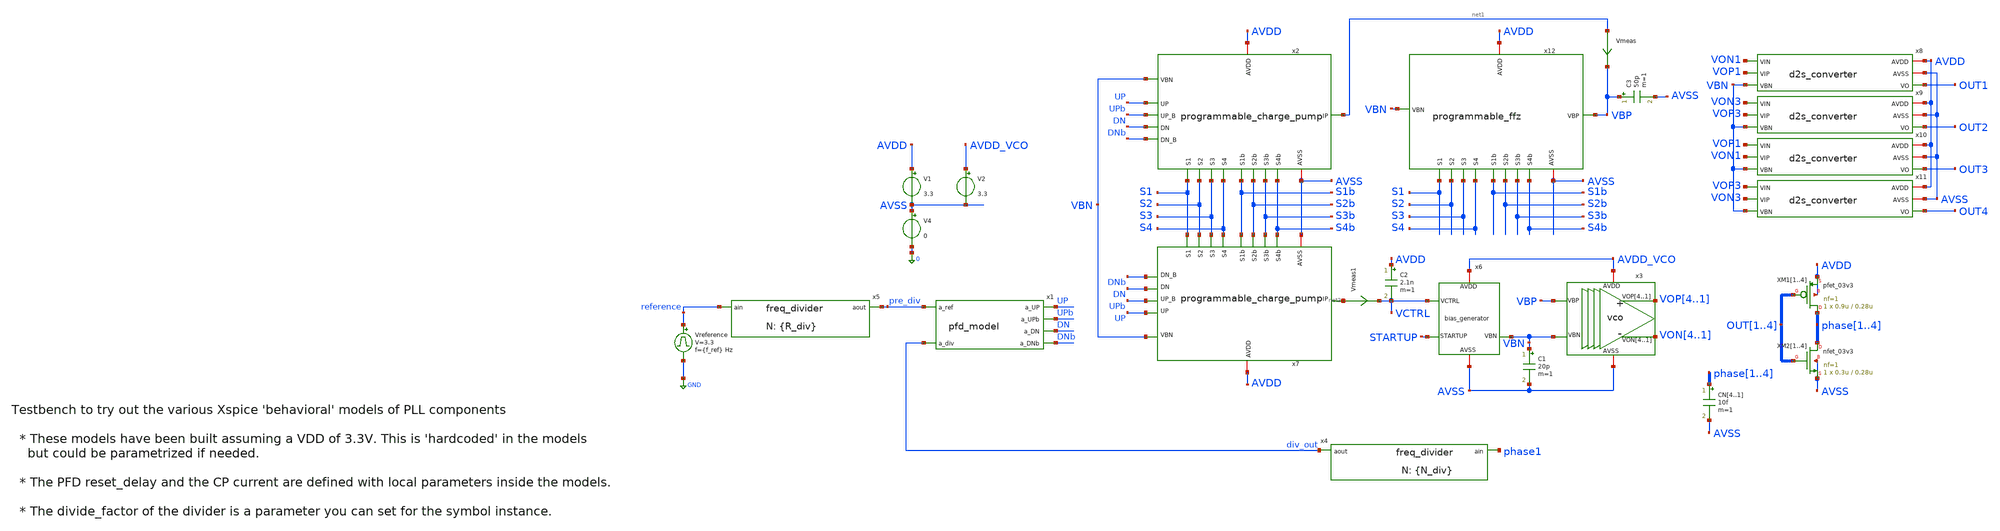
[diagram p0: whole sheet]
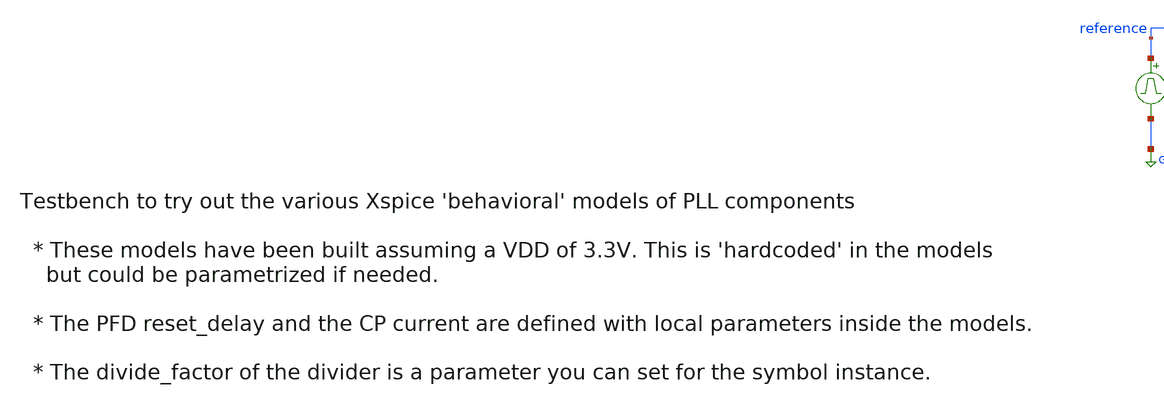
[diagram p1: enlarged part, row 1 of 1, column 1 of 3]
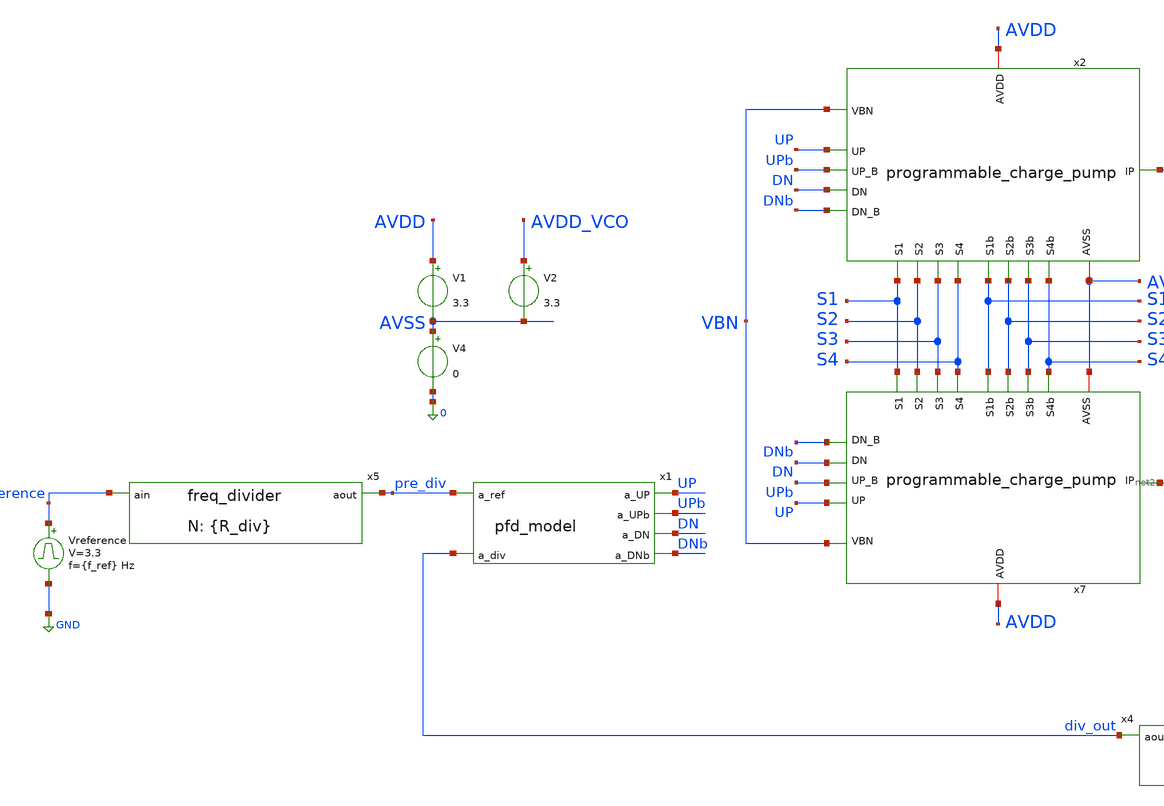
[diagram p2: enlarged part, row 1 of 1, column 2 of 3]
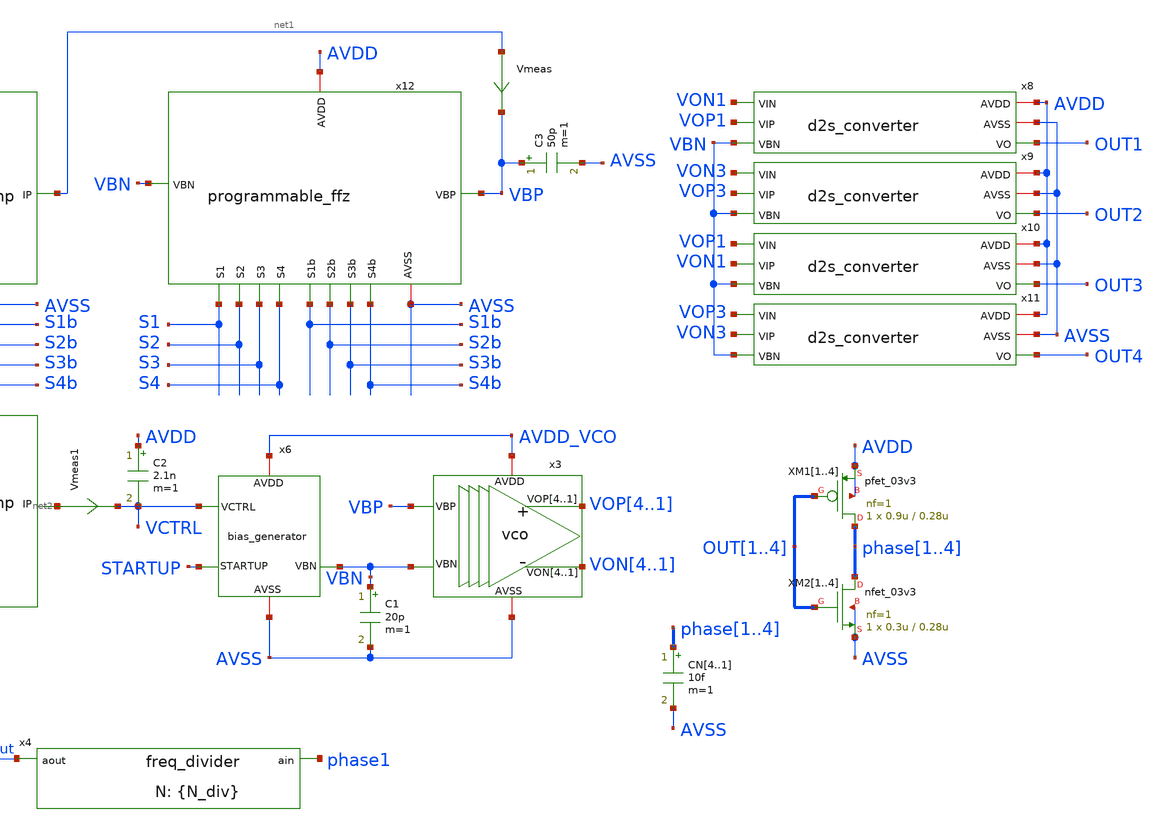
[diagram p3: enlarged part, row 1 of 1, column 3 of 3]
** sch_path: designs/libs/tb_pll/tb_PLL_CP_VCO_model.sch
**.subckt tb_PLL_CP_VCO_model
Vreference reference GND pulse 0 3.3 '0.495/ {f_ref} ' '0.01/{f_ref} ' '0.01/{f_ref} ' '0.49/{f_ref} '
+ '1/{f_ref} '
x1 pre_div UP UPb DN div_out DNb pfd_model
x4 div_out phase1 freq_divider divide_factor={N_div}
x5 pre_div reference freq_divider divide_factor={R_div}
x3 VOP4 VOP3 VOP2 VOP1 VON4 VON3 VON2 VON1 AVDD_VCO AVSS VBP VBN vco
x6 VCTRL AVDD_VCO STARTUP AVSS VBN bias_generator
C2 AVDD VCTRL 2.1n m=1
x8 AVDD AVSS VON1 VOP1 VBN OUT1 d2s_converter
XM11 phase1 OUT1 AVDD AVDD pfet_03v3 L=0.28u W=0.9u nf=1 ad='int((nf+1)/2) * W/nf * 0.18u' as='int((nf+2)/2) * W/nf * 0.18u'
+ pd='2*int((nf+1)/2) * (W/nf + 0.18u)' ps='2*int((nf+2)/2) * (W/nf + 0.18u)' nrd='0.18u / W' nrs='0.18u / W'
+ sa=0 sb=0 sd=0 m=1
XM12 phase2 OUT2 AVDD AVDD pfet_03v3 L=0.28u W=0.9u nf=1 ad='int((nf+1)/2) * W/nf * 0.18u' as='int((nf+2)/2) * W/nf * 0.18u'
+ pd='2*int((nf+1)/2) * (W/nf + 0.18u)' ps='2*int((nf+2)/2) * (W/nf + 0.18u)' nrd='0.18u / W' nrs='0.18u / W'
+ sa=0 sb=0 sd=0 m=1
XM13 phase3 OUT3 AVDD AVDD pfet_03v3 L=0.28u W=0.9u nf=1 ad='int((nf+1)/2) * W/nf * 0.18u' as='int((nf+2)/2) * W/nf * 0.18u'
+ pd='2*int((nf+1)/2) * (W/nf + 0.18u)' ps='2*int((nf+2)/2) * (W/nf + 0.18u)' nrd='0.18u / W' nrs='0.18u / W'
+ sa=0 sb=0 sd=0 m=1
XM14 phase4 OUT4 AVDD AVDD pfet_03v3 L=0.28u W=0.9u nf=1 ad='int((nf+1)/2) * W/nf * 0.18u' as='int((nf+2)/2) * W/nf * 0.18u'
+ pd='2*int((nf+1)/2) * (W/nf + 0.18u)' ps='2*int((nf+2)/2) * (W/nf + 0.18u)' nrd='0.18u / W' nrs='0.18u / W'
+ sa=0 sb=0 sd=0 m=1
XM21 phase1 OUT1 AVSS AVSS nfet_03v3 L=0.28u W=0.3u nf=1 ad='int((nf+1)/2) * W/nf * 0.18u' as='int((nf+2)/2) * W/nf * 0.18u'
+ pd='2*int((nf+1)/2) * (W/nf + 0.18u)' ps='2*int((nf+2)/2) * (W/nf + 0.18u)' nrd='0.18u / W' nrs='0.18u / W'
+ sa=0 sb=0 sd=0 m=1
XM22 phase2 OUT2 AVSS AVSS nfet_03v3 L=0.28u W=0.3u nf=1 ad='int((nf+1)/2) * W/nf * 0.18u' as='int((nf+2)/2) * W/nf * 0.18u'
+ pd='2*int((nf+1)/2) * (W/nf + 0.18u)' ps='2*int((nf+2)/2) * (W/nf + 0.18u)' nrd='0.18u / W' nrs='0.18u / W'
+ sa=0 sb=0 sd=0 m=1
XM23 phase3 OUT3 AVSS AVSS nfet_03v3 L=0.28u W=0.3u nf=1 ad='int((nf+1)/2) * W/nf * 0.18u' as='int((nf+2)/2) * W/nf * 0.18u'
+ pd='2*int((nf+1)/2) * (W/nf + 0.18u)' ps='2*int((nf+2)/2) * (W/nf + 0.18u)' nrd='0.18u / W' nrs='0.18u / W'
+ sa=0 sb=0 sd=0 m=1
XM24 phase4 OUT4 AVSS AVSS nfet_03v3 L=0.28u W=0.3u nf=1 ad='int((nf+1)/2) * W/nf * 0.18u' as='int((nf+2)/2) * W/nf * 0.18u'
+ pd='2*int((nf+1)/2) * (W/nf + 0.18u)' ps='2*int((nf+2)/2) * (W/nf + 0.18u)' nrd='0.18u / W' nrs='0.18u / W'
+ sa=0 sb=0 sd=0 m=1
x9 AVDD AVSS VON3 VOP3 VBN OUT2 d2s_converter
x10 AVDD AVSS VOP1 VON1 VBN OUT3 d2s_converter
x11 AVDD AVSS VOP3 VON3 VBN OUT4 d2s_converter
V1 AVDD AVSS 3.3
V4 AVSS 0 0
V2 AVDD_VCO AVSS 3.3
x2 AVSS AVDD UP UPb DN net1 DNb VBN S1b S1 S2b S2 S3b S3 S4b S4 programmable_charge_pump
x7 AVSS AVDD UP UPb DN net2 DNb VBN S1b S1 S2b S2 S3b S3 S4b S4 programmable_charge_pump
CN4 phase1 AVSS 10f m=1
CN3 phase2 AVSS 10f m=1
CN2 phase3 AVSS 10f m=1
CN1 phase4 AVSS 10f m=1
Vmeas net1 VBP 0
.save i(vmeas)
Vmeas1 net2 VCTRL 0
.save i(vmeas1)
C1 VBN AVSS 20p m=1
C3 VBP AVSS 50p m=1
x12 VBP AVSS AVDD VBN S1b S1 S2b S2 S3b S3 S4b S4 programmable_ffz
**** begin user architecture code


.param f_ref=2MEG R_div=2 N_div=255
*.param f_ref=2e3 R_div=2 N_div=255
.param tp_ref='1/f_ref' td_ref='tp_ref*2'
Vref reference gnd pulse(0 3.3 0 10p 10p tp_ref td_ref)

*.ic v(VCTRL)=2.6 v(vbp)=2.6
.ic v(VCTRL)=1 v(vbp)=1

.ic v(vop1)=3.3 v(von1)=0 v(startup)=0
.options reltol=1e-5 cshunt=1e-15
.options method=gear

.param d1=0 d2=0 d3=0 d4=0
.param d1b=3.3 d2b=3.3 d3b=3.3 d4b=3.3

*.param d1=3.3 d2=3.3 d3=3.3 d4=3.3
*.param d1b=0 d2b=0 d3b=0 d4b=0

VS1 S1 0 d1
VS2 S2 0 d2
VS3 S3 0 d3
VS4 S4 0 d4

VS1b S1b 0 d1b
VS2b S2b 0 d2b
VS3b S3b 0 d3b
VS4b S4b 0 d4b

.control
set wr_singlescale
set wr_vecnames

* save all
save v(VCTRL) v(vbp) v(vbn) v(reference) v(div_out) v(pre_div) v(phase1) v(phase2) v(phase3)
+ v(phase4) v(up) v(dn)

*v(vop1) v(von1) v(vop3) v(von3)

*OP
*show all

*tran 100n 70m
tran 0.1n 100u

remzerovec

*tran 1
*write tb_PLL_CP_VCO_model_R2_N2_350MEG.raw
*tran 2
write tb_PLL_CP_VCO_model_R2_N255_255MEG.raw

*tran 3
*write tb_PLL_CP_VCO_model_R2_N2_50kHz.raw
*tran 4
*write tb_PLL_CP_VCO_model_R2_N255_255kHz.raw
*write tb_PLL_CP_VCO_model_R2_N200_200kHz.raw
wrdata
+ /foss/designs/synchronos-chipathon-2026/designs/libs/scripts/sim_data/tb_PLL_CP_VCO_model_R2_N255_255MEG.txt tran.all
*tran 5

*tran 6

*tran 8

*tran 10

.endc



.include $::180MCU_MODELS/design.ngspice
.lib $::180MCU_MODELS/sm141064.ngspice typical
*.lib $::180MCU_MODELS/sm141064.ngspice SS
*.lib $::180MCU_MODELS/sm141064.ngspice FF
*.lib $::180MCU_MODELS/sm141064.ngspice SF
*.lib $::180MCU_MODELS/sm141064.ngspice FS

**** end user architecture code
**.ends

* expanding   symbol:  libs/model_pll/pfd_model.sym # of pins=6
** sym_path: designs/libs/model_pll/pfd_model.sym
** sch_path: designs/libs/model_pll/pfd_model.sch
.subckt pfd_model a_ref a_UP a_UPb a_DN a_div a_DNb
*.ipin a_ref
*.ipin a_div
*.opin a_UP
*.opin a_UPb
*.opin a_DN
*.opin a_DNb
* noconn a_ref
* noconn a_div
* noconn a_UP
* noconn a_UPb
* noconn a_DN
* noconn a_DNb
**** begin user architecture code


* PFD Model using digital Xspice components

* pfd_delay local parameter sets the duration of the overlap (dead-band elimination)
* Reduced from 10ns to 200ps to prevent massive Vctrl ripple
*.param pfd_delay = 200p
.param pfd_delay = 1.5n

** Digital 1 and 0 to drive Flip-Flops
aone 0 d_d1 d_inv
azero d_d1 d_d0 d_inv
.model d_inv d_inverter()

** Flip Flops
ad1 d_d1 d_R d_d0 d_rset d_U d_U_ flop1
ad2 d_d1 d_V d_d0 d_rset d_D d_D_ flop1
.model flop1 d_dff(clk_delay = 1.0e-10 set_delay = 1.0e-10  reset_delay = {pfd_delay} ic = 2 rise_delay
+ = 1.0e-10  fall_delay = 1e-10)

* AND Gate
aa1 [d_U d_D] d_rset and1
.model and1 d_and(rise_delay = 1e-10 fall_delay = 1e-10   input_load = 0.5e-12)

* WINDOW FIX: Widened thresholds to catch fast analog edges safely
aADC [ a_ref a_div ] [ d_R d_V ] adc_buff
.model adc_buff adc_bridge(in_low = 1.2 in_high = 2.1 rise_delay = 10p fall_delay = 10p)

* DAC FIX: Explicitly defined analog rise/fall times to prevent solver crashes
aDAC [ d_U d_U_ d_D d_D_ d_rset d_R d_V d_d1 d_d0 ] [ a_UP a_UPb a_DN a_DNb a_rset a_R a_V a_d1
+ a_d0] dac_buff
.model dac_buff dac_bridge(out_low = 0 out_high = 3.3 t_rise = 500p t_fall = 500p)


**** end user architecture code
.ends


* expanding   symbol:  libs/model_pll/freq_divider.sym # of pins=2
** sym_path: libs/model_pll/freq_divider.sym
** sch_path: libs/model_pll/freq_divider.sch
.subckt freq_divider aout ain  divide_factor=20
*.ipin ain
*.opin aout
* noconn ain
* noconn aout
**** begin user architecture code


* Behavioral Frequency Divider with robust Mixed-Signal Bridges

* Top-level parameter (Defaults to 10 if not passed by symbol)
.param divide_factor = 10

* MATH FIX: Guarantees at least 1 high cycle, targets 50% duty cycle
.param high_cycles = {max(1, floor(divide_factor/2))}

* Xspice digital frequency divider
adiv din dout divider
.model divider d_fdiv(div_factor = {divide_factor}  high_cycles = {high_cycles}  i_count = 0  rise_delay
+ = 10p fall_delay = 10p )

* WINDOW FIX: Widened analog-to-digital thresholds to catch fast sine waves
aADC [ ain ] [ din ] adc_buff
.model adc_buff adc_bridge(in_low = 1.2 in_high = 2.1 rise_delay = 10p fall_delay = 10p)

* Digital-to-analog bridge
aDAC [ dout ] [ aout ] dac_buff
.model dac_buff dac_bridge(out_low = 0 out_high = 3.3 t_rise = 10p t_fall = 10p)


**** end user architecture code
.ends


* expanding   symbol:  libs/core_analog/vco/vco.sym # of pins=6
** sym_path: designs/libs/core_analog/vco/vco.sym
** sch_path: designs/libs/core_analog/vco/vco.sch
.subckt vco VOP4 VOP3 VOP2 VOP1 VON4 VON3 VON2 VON1 AVDD AVSS VBP VBN
*.opin VOP1,VOP2,VOP3,VOP4
*.opin VON1,VON2,VON3,VON4
*.ipin VBP
*.ipin VBN
*.iopin AVDD
*.iopin AVSS
x1 VOP1 AVDD VOP4 VON4 VON1 AVSS VBP VBN delay_stage
x2 VOP2 AVDD VON1 VOP1 VON2 AVSS VBP VBN delay_stage
x3 VOP3 AVDD VON2 VOP2 VON3 AVSS VBP VBN delay_stage
x4 VOP4 AVDD VON3 VOP3 VON4 AVSS VBP VBN delay_stage
.ends


* expanding   symbol:  libs/core_analog/bias_generator/bias_generator.sym # of pins=5
** sym_path: designs/libs/core_analog/bias_generator/bias_generator.sym
** sch_path: designs/libs/core_analog/bias_generator/bias_generator.sch
.subckt bias_generator VCTRL AVDD STARTUP AVSS VBN
*.ipin VCTRL
*.ipin STARTUP
*.iopin AVDD
*.iopin AVSS
*.opin VBN
x1 VBN AVDD net2 VCTRL AVSS net1 ota_5t
XM1 net1 net1 AVDD AVDD pfet_03v3 L=0.5u W=16.8u nf=1 ad='int((nf+1)/2) * W/nf * 0.18u' as='int((nf+2)/2) * W/nf * 0.18u'
+ pd='2*int((nf+1)/2) * (W/nf + 0.18u)' ps='2*int((nf+2)/2) * (W/nf + 0.18u)' nrd='0.18u / W' nrs='0.18u / W'
+ sa=0 sb=0 sd=0 m=16
XM8 net2 AVDD net4 AVSS nfet_03v3 L=0.5u W=2.08u nf=1 ad='int((nf+1)/2) * W/nf * 0.18u' as='int((nf+2)/2) * W/nf * 0.18u'
+ pd='2*int((nf+1)/2) * (W/nf + 0.18u)' ps='2*int((nf+2)/2) * (W/nf + 0.18u)' nrd='0.18u / W' nrs='0.18u / W'
+ sa=0 sb=0 sd=0 m=8
XM11 net1 AVDD net3 AVSS nfet_03v3 L=0.5u W=2.08u nf=1 ad='int((nf+1)/2) * W/nf * 0.18u' as='int((nf+2)/2) * W/nf * 0.18u'
+ pd='2*int((nf+1)/2) * (W/nf + 0.18u)' ps='2*int((nf+2)/2) * (W/nf + 0.18u)' nrd='0.18u / W' nrs='0.18u / W'
+ sa=0 sb=0 sd=0 m=8
XM3 net4 VBN AVSS AVSS nfet_03v3 L=0.5u W=11.25u nf=1 ad='int((nf+1)/2) * W/nf * 0.18u' as='int((nf+2)/2) * W/nf * 0.18u'
+ pd='2*int((nf+1)/2) * (W/nf + 0.18u)' ps='2*int((nf+2)/2) * (W/nf + 0.18u)' nrd='0.18u / W' nrs='0.18u / W'
+ sa=0 sb=0 sd=0 m=8
XM4 net3 VBN AVSS AVSS nfet_03v3 L=0.5u W=11.25u nf=1 ad='int((nf+1)/2) * W/nf * 0.18u' as='int((nf+2)/2) * W/nf * 0.18u'
+ pd='2*int((nf+1)/2) * (W/nf + 0.18u)' ps='2*int((nf+2)/2) * (W/nf + 0.18u)' nrd='0.18u / W' nrs='0.18u / W'
+ sa=0 sb=0 sd=0 m=8
XM10 net3 STARTUP AVSS AVSS nfet_03v3 L=0.5u W=11.25u nf=1 ad='int((nf+1)/2) * W/nf * 0.18u' as='int((nf+2)/2) * W/nf * 0.18u'
+ pd='2*int((nf+1)/2) * (W/nf + 0.18u)' ps='2*int((nf+2)/2) * (W/nf + 0.18u)' nrd='0.18u / W' nrs='0.18u / W'
+ sa=0 sb=0 sd=0 m=8
XM2 net2 VCTRL AVDD AVDD pfet_03v3 L=1.5u W=1.1u nf=1 ad='int((nf+1)/2) * W/nf * 0.18u' as='int((nf+2)/2) * W/nf * 0.18u'
+ pd='2*int((nf+1)/2) * (W/nf + 0.18u)' ps='2*int((nf+2)/2) * (W/nf + 0.18u)' nrd='0.18u / W' nrs='0.18u / W'
+ sa=0 sb=0 sd=0 m=8
XM5 net2 net2 AVDD AVDD pfet_03v3 L=1.5u W=1.1u nf=1 ad='int((nf+1)/2) * W/nf * 0.18u' as='int((nf+2)/2) * W/nf * 0.18u'
+ pd='2*int((nf+1)/2) * (W/nf + 0.18u)' ps='2*int((nf+2)/2) * (W/nf + 0.18u)' nrd='0.18u / W' nrs='0.18u / W'
+ sa=0 sb=0 sd=0 m=8
.ends


* expanding   symbol:  libs/core_analog/d2s_converter/d2s_converter.sym # of pins=6
** sym_path: designs/libs/core_analog/d2s_converter/d2s_converter.sym
** sch_path: designs/libs/core_analog/d2s_converter/d2s_converter.sch
.subckt d2s_converter AVDD AVSS VIN VIP VBN VO
*.iopin AVDD
*.iopin AVSS
*.ipin VIN
*.ipin VIP
*.opin VO
*.ipin VBN
XM2 VOPB VIN i1 AVSS nfet_03v3 L=0.3u W=1.9u nf=1 ad='int((nf+1)/2) * W/nf * 0.18u' as='int((nf+2)/2) * W/nf * 0.18u'
+ pd='2*int((nf+1)/2) * (W/nf + 0.18u)' ps='2*int((nf+2)/2) * (W/nf + 0.18u)' nrd='0.18u / W' nrs='0.18u / W'
+ sa=0 sb=0 sd=0 m=4
XM4 VOPB VOPB AVDD AVDD pfet_03v3 L=0.3u W=1.4u nf=1 ad='int((nf+1)/2) * W/nf * 0.18u' as='int((nf+2)/2) * W/nf * 0.18u'
+ pd='2*int((nf+1)/2) * (W/nf + 0.18u)' ps='2*int((nf+2)/2) * (W/nf + 0.18u)' nrd='0.18u / W' nrs='0.18u / W'
+ sa=0 sb=0 sd=0 m=4
XM11 VOB VOB AVSS AVSS nfet_03v3 L=0.3u W=1.5u nf=1 ad='int((nf+1)/2) * W/nf * 0.18u' as='int((nf+2)/2) * W/nf * 0.18u'
+ pd='2*int((nf+1)/2) * (W/nf + 0.18u)' ps='2*int((nf+2)/2) * (W/nf + 0.18u)' nrd='0.18u / W' nrs='0.18u / W'
+ sa=0 sb=0 sd=0 m=4
XM13 VOB VOP AVDD AVDD pfet_03v3 L=0.3u W=2u nf=1 ad='int((nf+1)/2) * W/nf * 0.18u' as='int((nf+2)/2) * W/nf * 0.18u'
+ pd='2*int((nf+1)/2) * (W/nf + 0.18u)' ps='2*int((nf+2)/2) * (W/nf + 0.18u)' nrd='0.18u / W' nrs='0.18u / W'
+ sa=0 sb=0 sd=0 m=4
XM3 VOP VIP i1 AVSS nfet_03v3 L=0.3u W=1.9u nf=1 ad='int((nf+1)/2) * W/nf * 0.18u' as='int((nf+2)/2) * W/nf * 0.18u'
+ pd='2*int((nf+1)/2) * (W/nf + 0.18u)' ps='2*int((nf+2)/2) * (W/nf + 0.18u)' nrd='0.18u / W' nrs='0.18u / W'
+ sa=0 sb=0 sd=0 m=4
XM5 VOP VOPB AVDD AVDD pfet_03v3 L=0.3u W=1.4u nf=1 ad='int((nf+1)/2) * W/nf * 0.18u' as='int((nf+2)/2) * W/nf * 0.18u'
+ pd='2*int((nf+1)/2) * (W/nf + 0.18u)' ps='2*int((nf+2)/2) * (W/nf + 0.18u)' nrd='0.18u / W' nrs='0.18u / W'
+ sa=0 sb=0 sd=0 m=4
XM7 VONB VIP i2 AVSS nfet_03v3 L=0.3u W=1.9u nf=1 ad='int((nf+1)/2) * W/nf * 0.18u' as='int((nf+2)/2) * W/nf * 0.18u'
+ pd='2*int((nf+1)/2) * (W/nf + 0.18u)' ps='2*int((nf+2)/2) * (W/nf + 0.18u)' nrd='0.18u / W' nrs='0.18u / W'
+ sa=0 sb=0 sd=0 m=4
XM8 VONB VONB AVDD AVDD pfet_03v3 L=0.3u W=1.4u nf=1 ad='int((nf+1)/2) * W/nf * 0.18u' as='int((nf+2)/2) * W/nf * 0.18u'
+ pd='2*int((nf+1)/2) * (W/nf + 0.18u)' ps='2*int((nf+2)/2) * (W/nf + 0.18u)' nrd='0.18u / W' nrs='0.18u / W'
+ sa=0 sb=0 sd=0 m=4
XM9 VON VIN i2 AVSS nfet_03v3 L=0.3u W=1.9u nf=1 ad='int((nf+1)/2) * W/nf * 0.18u' as='int((nf+2)/2) * W/nf * 0.18u'
+ pd='2*int((nf+1)/2) * (W/nf + 0.18u)' ps='2*int((nf+2)/2) * (W/nf + 0.18u)' nrd='0.18u / W' nrs='0.18u / W'
+ sa=0 sb=0 sd=0 m=4
XM10 VON VONB AVDD AVDD pfet_03v3 L=0.3u W=1.4u nf=1 ad='int((nf+1)/2) * W/nf * 0.18u' as='int((nf+2)/2) * W/nf * 0.18u'
+ pd='2*int((nf+1)/2) * (W/nf + 0.18u)' ps='2*int((nf+2)/2) * (W/nf + 0.18u)' nrd='0.18u / W' nrs='0.18u / W'
+ sa=0 sb=0 sd=0 m=4
XM14 VO VON AVDD AVDD pfet_03v3 L=0.3u W=2u nf=1 ad='int((nf+1)/2) * W/nf * 0.18u' as='int((nf+2)/2) * W/nf * 0.18u'
+ pd='2*int((nf+1)/2) * (W/nf + 0.18u)' ps='2*int((nf+2)/2) * (W/nf + 0.18u)' nrd='0.18u / W' nrs='0.18u / W'
+ sa=0 sb=0 sd=0 m=4
XM12 VO VOB AVSS AVSS nfet_03v3 L=0.3u W=1.5u nf=1 ad='int((nf+1)/2) * W/nf * 0.18u' as='int((nf+2)/2) * W/nf * 0.18u'
+ pd='2*int((nf+1)/2) * (W/nf + 0.18u)' ps='2*int((nf+2)/2) * (W/nf + 0.18u)' nrd='0.18u / W' nrs='0.18u / W'
+ sa=0 sb=0 sd=0 m=4
XM1 i1 VBN AVSS AVSS nfet_03v3 L=0.5u W=11.25u nf=1 ad='int((nf+1)/2) * W/nf * 0.18u' as='int((nf+2)/2) * W/nf * 0.18u'
+ pd='2*int((nf+1)/2) * (W/nf + 0.18u)' ps='2*int((nf+2)/2) * (W/nf + 0.18u)' nrd='0.18u / W' nrs='0.18u / W'
+ sa=0 sb=0 sd=0 m=4
XM6 i2 VBN AVSS AVSS nfet_03v3 L=0.5u W=11.25u nf=1 ad='int((nf+1)/2) * W/nf * 0.18u' as='int((nf+2)/2) * W/nf * 0.18u'
+ pd='2*int((nf+1)/2) * (W/nf + 0.18u)' ps='2*int((nf+2)/2) * (W/nf + 0.18u)' nrd='0.18u / W' nrs='0.18u / W'
+ sa=0 sb=0 sd=0 m=4
.ends


* expanding   symbol:  libs/core_analog/programmable_charge_pump/programmable_charge_pump.sym # of
*+ pins=16
** sym_path: designs/libs/core_analog/programmable_charge_pump/programmable_charge_pump.sym
** sch_path: designs/libs/core_analog/programmable_charge_pump/programmable_charge_pump.sch
.subckt programmable_charge_pump AVSS AVDD UP UP_B DN IP DN_B VBN S1b S1 S2b S2 S3b S3 S4b S4
*.ipin VBN
*.ipin S1b
*.ipin S1
*.ipin S2b
*.ipin S2
*.ipin S3b
*.ipin S3
*.ipin S4b
*.ipin S4
*.iopin AVSS
*.iopin AVDD
*.ipin UP
*.ipin UP_B
*.ipin DN
*.ipin DN_B
*.opin IP
x1 AVDD AVSS UP UP_B DN DN_B VBN1 IP S1b charge_pump
x61 AVDD AVSS UP UP_B DN DN_B VBN2 IP S2b charge_pump
x62 AVDD AVSS UP UP_B DN DN_B VBN2 IP S2b charge_pump
x71 AVDD AVSS UP UP_B DN DN_B VBN3 IP S3b charge_pump
x72 AVDD AVSS UP UP_B DN DN_B VBN3 IP S3b charge_pump
x73 AVDD AVSS UP UP_B DN DN_B VBN3 IP S3b charge_pump
x74 AVDD AVSS UP UP_B DN DN_B VBN3 IP S3b charge_pump
x81 AVDD AVSS UP UP_B DN DN_B VBN4 IP S4b charge_pump
x82 AVDD AVSS UP UP_B DN DN_B VBN4 IP S4b charge_pump
x83 AVDD AVSS UP UP_B DN DN_B VBN4 IP S4b charge_pump
x84 AVDD AVSS UP UP_B DN DN_B VBN4 IP S4b charge_pump
x85 AVDD AVSS UP UP_B DN DN_B VBN4 IP S4b charge_pump
x86 AVDD AVSS UP UP_B DN DN_B VBN4 IP S4b charge_pump
x87 AVDD AVSS UP UP_B DN DN_B VBN4 IP S4b charge_pump
x88 AVDD AVSS UP UP_B DN DN_B VBN4 IP S4b charge_pump
x2 VBN AVSS S1 VBN1 S1b AVDD transmission_gate
x0 AVDD AVSS UP UP_B DN DN_B VBN IP AVSS charge_pump
x3 VBN AVSS S2 VBN2 S2b AVDD transmission_gate
x4 VBN AVSS S3 VBN3 S3b AVDD transmission_gate
x5 VBN AVSS S4 VBN4 S4b AVDD transmission_gate
.ends


* expanding   symbol:  libs/core_analog/programmable_ffz/programmable_ffz.sym # of pins=12
** sym_path: designs/libs/core_analog/programmable_ffz/programmable_ffz.sym
** sch_path: designs/libs/core_analog/programmable_ffz/programmable_ffz.sch
.subckt programmable_ffz VBP AVSS AVDD VBN S1b S1 S2b S2 S3b S3 S4b S4
*.ipin VBN
*.ipin S1b
*.ipin S1
*.ipin S2b
*.ipin S2
*.ipin S3b
*.ipin S3
*.ipin S4b
*.ipin S4
*.iopin AVSS
*.iopin AVDD
*.opin VBP
x2 VBN AVSS S1 VBN1 S1b AVDD transmission_gate
x3 VBN AVSS S2 VBN2 S2b AVDD transmission_gate
x4 VBN AVSS S3 VBN3 S3b AVDD transmission_gate
x5 VBN AVSS S4 VBN4 S4b AVDD transmission_gate
x1 AVDD VBP VBN AVSS AVSS feed_forward_zero
x6 AVDD net1 VBN1 S1b AVSS feed_forward_zero
x71 AVDD net2 VBN2 S2b AVSS feed_forward_zero
x72 AVDD net2 VBN2 S2b AVSS feed_forward_zero
x11 AVDD net3 VBN3 S3b AVSS feed_forward_zero
x12 AVDD net3 VBN3 S3b AVSS feed_forward_zero
x13 AVDD net3 VBN3 S3b AVSS feed_forward_zero
x14 AVDD net3 VBN3 S3b AVSS feed_forward_zero
x21 AVDD net4 VBN4 S4b AVSS feed_forward_zero
x22 AVDD net4 VBN4 S4b AVSS feed_forward_zero
x23 AVDD net4 VBN4 S4b AVSS feed_forward_zero
x24 AVDD net4 VBN4 S4b AVSS feed_forward_zero
x25 AVDD net4 VBN4 S4b AVSS feed_forward_zero
x26 AVDD net4 VBN4 S4b AVSS feed_forward_zero
x27 AVDD net4 VBN4 S4b AVSS feed_forward_zero
x28 AVDD net4 VBN4 S4b AVSS feed_forward_zero
x7 net1 AVSS S1 VBP S1b AVDD transmission_gate
x8 net2 AVSS S2 VBP S2b AVDD transmission_gate
x9 net3 AVSS S3 VBP S3b AVDD transmission_gate
x10 net4 AVSS S4 VBP S4b AVDD transmission_gate
.ends


* expanding   symbol:  libs/core_analog/delay_stage/delay_stage.sym # of pins=8
** sym_path: designs/libs/core_analog/delay_stage/delay_stage.sym
** sch_path: designs/libs/core_analog/delay_stage/delay_stage.sch
.subckt delay_stage VOP AVDD VIP VIN VON AVSS VBP VBN
*.ipin VIP
*.ipin VIN
*.opin VOP
*.opin VON
*.iopin AVDD
*.iopin AVSS
*.ipin VBP
*.ipin VBN
XM5 VON VIP net1 AVSS nfet_03v3 L=0.5u W=2.08u nf=1 ad='int((nf+1)/2) * W/nf * 0.18u' as='int((nf+2)/2) * W/nf * 0.18u'
+ pd='2*int((nf+1)/2) * (W/nf + 0.18u)' ps='2*int((nf+2)/2) * (W/nf + 0.18u)' nrd='0.18u / W' nrs='0.18u / W'
+ sa=0 sb=0 sd=0 m=8
XM2 VON VON AVDD AVDD pfet_03v3 L=1.5u W=1.1u nf=1 ad='int((nf+1)/2) * W/nf * 0.18u' as='int((nf+2)/2) * W/nf * 0.18u'
+ pd='2*int((nf+1)/2) * (W/nf + 0.18u)' ps='2*int((nf+2)/2) * (W/nf + 0.18u)' nrd='0.18u / W' nrs='0.18u / W'
+ sa=0 sb=0 sd=0 m=8
XM6 VOP VIN net1 AVSS nfet_03v3 L=0.5u W=2.08u nf=1 ad='int((nf+1)/2) * W/nf * 0.18u' as='int((nf+2)/2) * W/nf * 0.18u'
+ pd='2*int((nf+1)/2) * (W/nf + 0.18u)' ps='2*int((nf+2)/2) * (W/nf + 0.18u)' nrd='0.18u / W' nrs='0.18u / W'
+ sa=0 sb=0 sd=0 m=8
XM1 VON VBP AVDD AVDD pfet_03v3 L=1.5u W=1.1u nf=1 ad='int((nf+1)/2) * W/nf * 0.18u' as='int((nf+2)/2) * W/nf * 0.18u'
+ pd='2*int((nf+1)/2) * (W/nf + 0.18u)' ps='2*int((nf+2)/2) * (W/nf + 0.18u)' nrd='0.18u / W' nrs='0.18u / W'
+ sa=0 sb=0 sd=0 m=8
XM3 VOP VBP AVDD AVDD pfet_03v3 L=1.5u W=1.1u nf=1 ad='int((nf+1)/2) * W/nf * 0.18u' as='int((nf+2)/2) * W/nf * 0.18u'
+ pd='2*int((nf+1)/2) * (W/nf + 0.18u)' ps='2*int((nf+2)/2) * (W/nf + 0.18u)' nrd='0.18u / W' nrs='0.18u / W'
+ sa=0 sb=0 sd=0 m=8
XM4 VOP VOP AVDD AVDD pfet_03v3 L=1.5u W=1.1u nf=1 ad='int((nf+1)/2) * W/nf * 0.18u' as='int((nf+2)/2) * W/nf * 0.18u'
+ pd='2*int((nf+1)/2) * (W/nf + 0.18u)' ps='2*int((nf+2)/2) * (W/nf + 0.18u)' nrd='0.18u / W' nrs='0.18u / W'
+ sa=0 sb=0 sd=0 m=8
XM8 net1 VBN AVSS AVSS nfet_03v3 L=0.5u W=11.25u nf=1 ad='int((nf+1)/2) * W/nf * 0.18u' as='int((nf+2)/2) * W/nf * 0.18u'
+ pd='2*int((nf+1)/2) * (W/nf + 0.18u)' ps='2*int((nf+2)/2) * (W/nf + 0.18u)' nrd='0.18u / W' nrs='0.18u / W'
+ sa=0 sb=0 sd=0 m=8
.ends


* expanding   symbol:  libs/core_analog/ota_5t/ota_5t.sym # of pins=6
** sym_path: designs/libs/core_analog/ota_5t/ota_5t.sym
** sch_path: designs/libs/core_analog/ota_5t/ota_5t.sch
.subckt ota_5t VO AVDD VI+ VI- AVSS VB
*.ipin VI+
*.ipin VI-
*.ipin VB
*.iopin AVDD
*.iopin AVSS
*.opin VO
XM1 VO VI- net2 AVDD pfet_03v3 L=0.5u W=6.55u nf=1 ad='int((nf+1)/2) * W/nf * 0.18u' as='int((nf+2)/2) * W/nf * 0.18u'
+ pd='2*int((nf+1)/2) * (W/nf + 0.18u)' ps='2*int((nf+2)/2) * (W/nf + 0.18u)' nrd='0.18u / W' nrs='0.18u / W'
+ sa=0 sb=0 sd=0 m=8
XM4 VO net1 AVSS AVSS nfet_03v3 L=0.5u W=4.8u nf=1 ad='int((nf+1)/2) * W/nf * 0.18u' as='int((nf+2)/2) * W/nf * 0.18u'
+ pd='2*int((nf+1)/2) * (W/nf + 0.18u)' ps='2*int((nf+2)/2) * (W/nf + 0.18u)' nrd='0.18u / W' nrs='0.18u / W'
+ sa=0 sb=0 sd=0 m=4
XM3 net2 VB net3 AVDD pfet_03v3 L=0.5u W=8.3u nf=1 ad='int((nf+1)/2) * W/nf * 0.18u' as='int((nf+2)/2) * W/nf * 0.18u'
+ pd='2*int((nf+1)/2) * (W/nf + 0.18u)' ps='2*int((nf+2)/2) * (W/nf + 0.18u)' nrd='0.18u / W' nrs='0.18u / W'
+ sa=0 sb=0 sd=0 m=16
XM2 net1 VI+ net2 AVDD pfet_03v3 L=0.5u W=6.55u nf=1 ad='int((nf+1)/2) * W/nf * 0.18u' as='int((nf+2)/2) * W/nf * 0.18u'
+ pd='2*int((nf+1)/2) * (W/nf + 0.18u)' ps='2*int((nf+2)/2) * (W/nf + 0.18u)' nrd='0.18u / W' nrs='0.18u / W'
+ sa=0 sb=0 sd=0 m=8
XM5 net1 net1 AVSS AVSS nfet_03v3 L=0.5u W=4.8u nf=1 ad='int((nf+1)/2) * W/nf * 0.18u' as='int((nf+2)/2) * W/nf * 0.18u'
+ pd='2*int((nf+1)/2) * (W/nf + 0.18u)' ps='2*int((nf+2)/2) * (W/nf + 0.18u)' nrd='0.18u / W' nrs='0.18u / W'
+ sa=0 sb=0 sd=0 m=4
Vmeas AVDD net3 0
.save i(vmeas)
.ends


* expanding   symbol:  libs/core_analog/charge_pump/charge_pump.sym # of pins=9
** sym_path: designs/libs/core_analog/charge_pump/charge_pump.sym
** sch_path: designs/libs/core_analog/charge_pump/charge_pump.sch
.subckt charge_pump VDD VSS UP UP_B DN DN_B VBN IP S
*.iopin VDD
*.iopin VSS
*.ipin UP
*.ipin UP_B
*.ipin DN
*.ipin DN_B
*.ipin VBN
*.iopin IP
*.ipin S
x1 net5 net5 VDD net5 VDD cp_sym_load
x2 net3 net3 VDD net3 VDD cp_sym_load
x3 net4 net4 VDD net4 VDD cp_sym_load
x4 net5 net5 VDD IP VDD cp_sym_load
XM1 net1 VBN VSS VSS nfet_03v3 L=0.5u W=11.25u nf=1 ad='int((nf+1)/2) * W/nf * 0.18u' as='int((nf+2)/2) * W/nf * 0.18u'
+ pd='2*int((nf+1)/2) * (W/nf + 0.18u)' ps='2*int((nf+2)/2) * (W/nf + 0.18u)' nrd='0.18u / W' nrs='0.18u / W'
+ sa=0 sb=0 sd=0 m=1
XM3 net5 DN net1 VSS nfet_03v3 L=0.5u W=2.08u nf=1 ad='int((nf+1)/2) * W/nf * 0.18u' as='int((nf+2)/2) * W/nf * 0.18u'
+ pd='2*int((nf+1)/2) * (W/nf + 0.18u)' ps='2*int((nf+2)/2) * (W/nf + 0.18u)' nrd='0.18u / W' nrs='0.18u / W'
+ sa=0 sb=0 sd=0 m=1
XM7 VBN S VSS VSS nfet_03v3 L=0.5u W=1u nf=1 ad='int((nf+1)/2) * W/nf * 0.18u' as='int((nf+2)/2) * W/nf * 0.18u'
+ pd='2*int((nf+1)/2) * (W/nf + 0.18u)' ps='2*int((nf+2)/2) * (W/nf + 0.18u)' nrd='0.18u / W' nrs='0.18u / W'
+ sa=0 sb=0 sd=0 m=1
XM8 VBN S VSS VSS nfet_03v3 L=0.5u W=1u nf=1 ad='int((nf+1)/2) * W/nf * 0.18u' as='int((nf+2)/2) * W/nf * 0.18u'
+ pd='2*int((nf+1)/2) * (W/nf + 0.18u)' ps='2*int((nf+2)/2) * (W/nf + 0.18u)' nrd='0.18u / W' nrs='0.18u / W'
+ sa=0 sb=0 sd=0 m=1
XM4 net3 DN_B net1 VSS nfet_03v3 L=0.5u W=2.08u nf=1 ad='int((nf+1)/2) * W/nf * 0.18u' as='int((nf+2)/2) * W/nf * 0.18u'
+ pd='2*int((nf+1)/2) * (W/nf + 0.18u)' ps='2*int((nf+2)/2) * (W/nf + 0.18u)' nrd='0.18u / W' nrs='0.18u / W'
+ sa=0 sb=0 sd=0 m=1
XM5 net4 UP_B net2 VSS nfet_03v3 L=0.5u W=2.08u nf=1 ad='int((nf+1)/2) * W/nf * 0.18u' as='int((nf+2)/2) * W/nf * 0.18u'
+ pd='2*int((nf+1)/2) * (W/nf + 0.18u)' ps='2*int((nf+2)/2) * (W/nf + 0.18u)' nrd='0.18u / W' nrs='0.18u / W'
+ sa=0 sb=0 sd=0 m=1
XM6 IP UP net2 VSS nfet_03v3 L=0.5u W=2.08u nf=1 ad='int((nf+1)/2) * W/nf * 0.18u' as='int((nf+2)/2) * W/nf * 0.18u'
+ pd='2*int((nf+1)/2) * (W/nf + 0.18u)' ps='2*int((nf+2)/2) * (W/nf + 0.18u)' nrd='0.18u / W' nrs='0.18u / W'
+ sa=0 sb=0 sd=0 m=1
XM2 net2 VBN VSS VSS nfet_03v3 L=0.5u W=11.25u nf=1 ad='int((nf+1)/2) * W/nf * 0.18u' as='int((nf+2)/2) * W/nf * 0.18u'
+ pd='2*int((nf+1)/2) * (W/nf + 0.18u)' ps='2*int((nf+2)/2) * (W/nf + 0.18u)' nrd='0.18u / W' nrs='0.18u / W'
+ sa=0 sb=0 sd=0 m=1
.ends


* expanding   symbol:  libs/core_analog/transmission_gate/transmission_gate.sym # of pins=6
** sym_path: designs/libs/core_analog/transmission_gate/transmission_gate.sym
** sch_path: designs/libs/core_analog/transmission_gate/transmission_gate.sch
.subckt transmission_gate ind vss clkn ins clkp vdd
*.iopin ind
*.iopin ins
*.iopin clkn
*.iopin clkp
*.iopin vdd
*.iopin vss
XM1 ind clkp ins vdd pfet_03v3 L=0.5u W=3.0u nf=1 ad='int((nf+1)/2) * W/nf * 0.18u' as='int((nf+2)/2) * W/nf * 0.18u'
+ pd='2*int((nf+1)/2) * (W/nf + 0.18u)' ps='2*int((nf+2)/2) * (W/nf + 0.18u)' nrd='0.18u / W' nrs='0.18u / W'
+ sa=0 sb=0 sd=0 m=1
XM2 ind clkn ins vss nfet_03v3 L=0.5u W=1.0u nf=1 ad='int((nf+1)/2) * W/nf * 0.18u' as='int((nf+2)/2) * W/nf * 0.18u'
+ pd='2*int((nf+1)/2) * (W/nf + 0.18u)' ps='2*int((nf+2)/2) * (W/nf + 0.18u)' nrd='0.18u / W' nrs='0.18u / W'
+ sa=0 sb=0 sd=0 m=1
.ends


* expanding   symbol:  libs/core_analog/feed_forward_zero/feed_forward_zero.sym # of pins=5
** sym_path: designs/libs/core_analog/feed_forward_zero/feed_forward_zero.sym
** sch_path: designs/libs/core_analog/feed_forward_zero/feed_forward_zero.sch
.subckt feed_forward_zero AVDD VBP VBN S AVSS
*.opin VBP
*.iopin AVDD
*.iopin AVSS
*.ipin VBN
*.ipin S
XM1 VBP VBP AVDD AVDD pfet_03v3 L=1.5u W=1.1u nf=1 ad='int((nf+1)/2) * W/nf * 0.18u' as='int((nf+2)/2) * W/nf * 0.18u'
+ pd='2*int((nf+1)/2) * (W/nf + 0.18u)' ps='2*int((nf+2)/2) * (W/nf + 0.18u)' nrd='0.18u / W' nrs='0.18u / W'
+ sa=0 sb=0 sd=0 m=2
XM2 VBP VBP AVDD AVDD pfet_03v3 L=1.5u W=1.1u nf=1 ad='int((nf+1)/2) * W/nf * 0.18u' as='int((nf+2)/2) * W/nf * 0.18u'
+ pd='2*int((nf+1)/2) * (W/nf + 0.18u)' ps='2*int((nf+2)/2) * (W/nf + 0.18u)' nrd='0.18u / W' nrs='0.18u / W'
+ sa=0 sb=0 sd=0 m=2
XM3 VBP AVDD net1 AVSS nfet_03v3 L=0.5u W=2.08u nf=1 ad='int((nf+1)/2) * W/nf * 0.18u' as='int((nf+2)/2) * W/nf * 0.18u'
+ pd='2*int((nf+1)/2) * (W/nf + 0.18u)' ps='2*int((nf+2)/2) * (W/nf + 0.18u)' nrd='0.18u / W' nrs='0.18u / W'
+ sa=0 sb=0 sd=0 m=2
XM4 net1 VBN AVSS AVSS nfet_03v3 L=0.5u W=11.25u nf=1 ad='int((nf+1)/2) * W/nf * 0.18u' as='int((nf+2)/2) * W/nf * 0.18u'
+ pd='2*int((nf+1)/2) * (W/nf + 0.18u)' ps='2*int((nf+2)/2) * (W/nf + 0.18u)' nrd='0.18u / W' nrs='0.18u / W'
+ sa=0 sb=0 sd=0 m=2
XM7 VBN S AVSS AVSS nfet_03v3 L=0.5u W=1u nf=1 ad='int((nf+1)/2) * W/nf * 0.18u' as='int((nf+2)/2) * W/nf * 0.18u'
+ pd='2*int((nf+1)/2) * (W/nf + 0.18u)' ps='2*int((nf+2)/2) * (W/nf + 0.18u)' nrd='0.18u / W' nrs='0.18u / W'
+ sa=0 sb=0 sd=0 m=1
.ends


* expanding   symbol:  libs/core_analog/cp_sym_load/cp_sym_load.sym # of pins=5
** sym_path: designs/libs/core_analog/cp_sym_load/cp_sym_load.sym
** sch_path: designs/libs/core_analog/cp_sym_load/cp_sym_load.sch
.subckt cp_sym_load G1 G2 S D VDD
*.ipin G1
*.ipin G2
*.iopin S
*.iopin D
*.iopin VDD
XM1 D G1 S VDD pfet_03v3 L=1.5u W=1.1u nf=1 ad='int((nf+1)/2) * W/nf * 0.18u' as='int((nf+2)/2) * W/nf * 0.18u'
+ pd='2*int((nf+1)/2) * (W/nf + 0.18u)' ps='2*int((nf+2)/2) * (W/nf + 0.18u)' nrd='0.18u / W' nrs='0.18u / W'
+ sa=0 sb=0 sd=0 m=1
XM2 D G2 S VDD pfet_03v3 L=1.5u W=1.1u nf=1 ad='int((nf+1)/2) * W/nf * 0.18u' as='int((nf+2)/2) * W/nf * 0.18u'
+ pd='2*int((nf+1)/2) * (W/nf + 0.18u)' ps='2*int((nf+2)/2) * (W/nf + 0.18u)' nrd='0.18u / W' nrs='0.18u / W'
+ sa=0 sb=0 sd=0 m=1
.ends

.GLOBAL GND
.end
